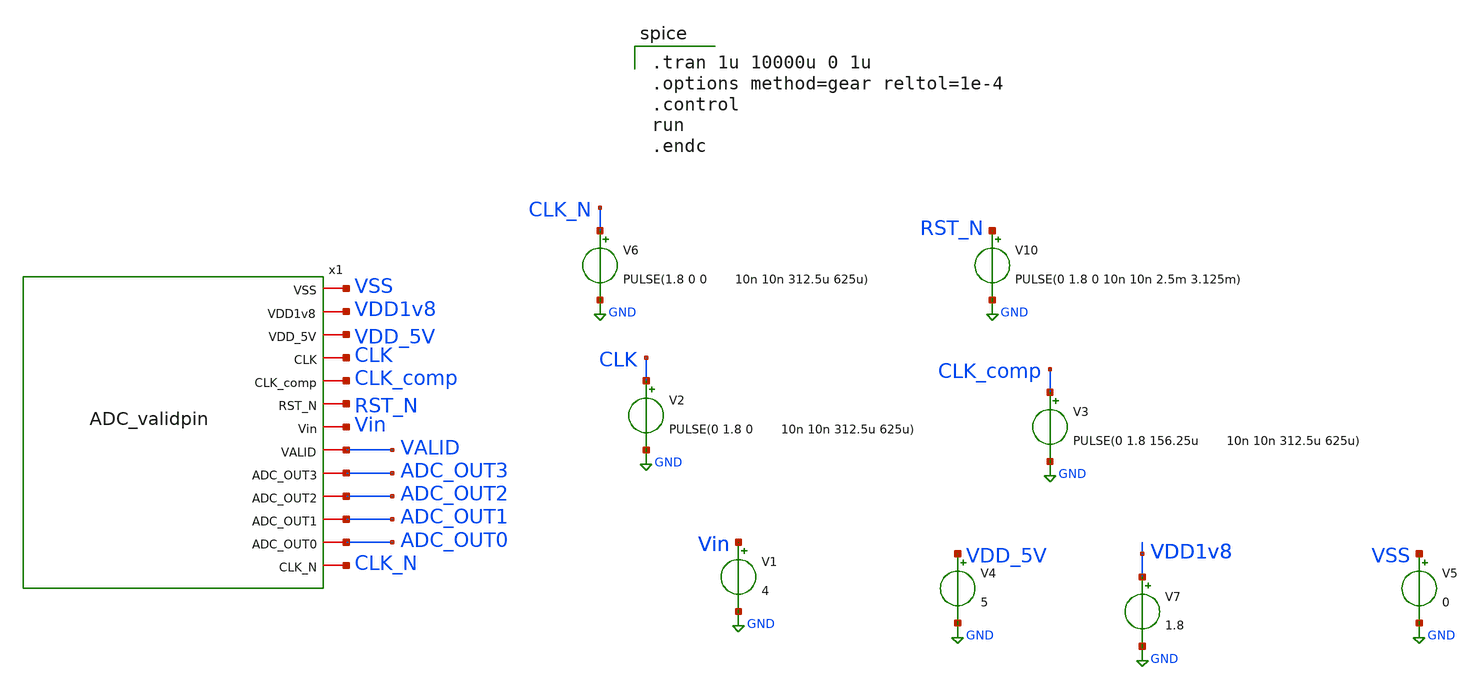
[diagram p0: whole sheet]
** sch_path: ADC/16bit_C2C/MagicAndSpice/ADC_validpin_TB.sch
**.subckt ADC_validpin_TB
x1 VSS VDD1v8 VDD_5V CLK CLK_comp RST_N Vin VALID ADC_OUT3 ADC_OUT2 ADC_OUT1 ADC_OUT0 CLK_N
+ ADC_validpin
V2 CLK GND PULSE(0 1.8 0 10n 10n 312.5u 625u)
V3 CLK_comp GND PULSE(0 1.8 156.25u 10n 10n 312.5u 625u)
V10 RST_N GND PULSE(0 1.8 0 10n 10n 2.5m 3.125m)
V1 Vin GND 4
V4 VDD_5V GND 5
V7 VDD1v8 GND 1.8
V5 VSS GND 0
V6 CLK_N GND PULSE(1.8 0 0 10n 10n 312.5u 625u)
**** begin user architecture code

** opencircuitdesign pdks install
.lib $::SKYWATER_MODELS/sky130.lib.spice tt



.tran 1u 10000u 0 1u
.options method=gear reltol=1e-4
.control
run
.endc

**** end user architecture code
**.ends
.GLOBAL GND
.end
